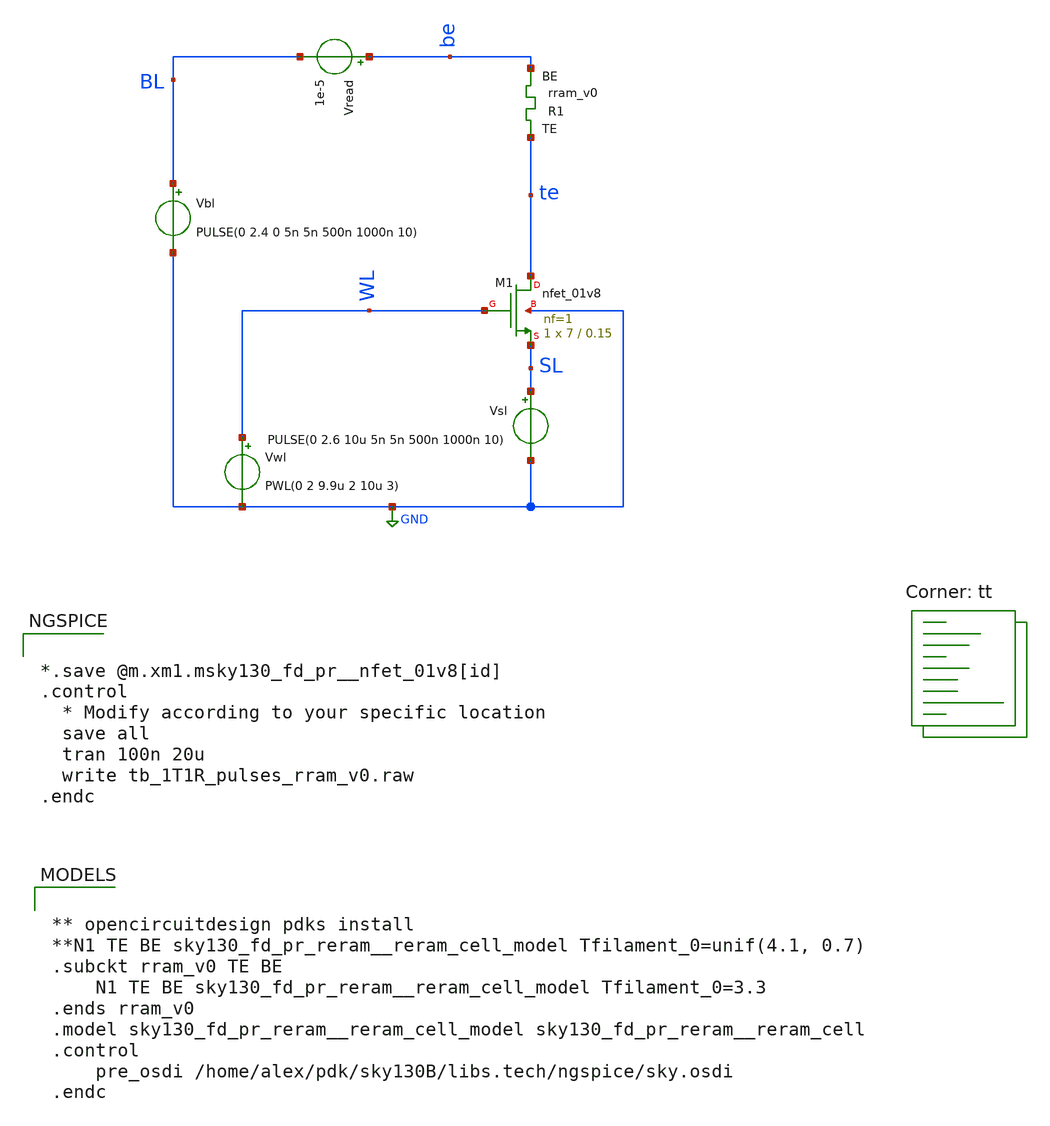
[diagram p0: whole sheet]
** sch_path: memristor_models/rram_london/tb_1T1R_pulses_sky.sch
**.subckt tb_1T1R_pulses_sky
XM1 te WL SL GND sky130_fd_pr__nfet_01v8 L=0.15 W=7 nf=1 ad='int((nf+1)/2) * W/nf * 0.29' as='int((nf+2)/2) * W/nf * 0.29'
+ pd='2*int((nf+1)/2) * (W/nf + 0.29)' ps='2*int((nf+2)/2) * (W/nf + 0.29)' nrd='0.29 / W' nrs='0.29 / W'
+ sa=0 sb=0 sd=0 mult=1 m=1
Vwl WL GND PWL(0 2 9.9u 2 10u 3)
Vbl BL GND PULSE(0 2.4 0 5n 5n 500n 1000n 10)
Vread be BL 1e-5
XR1 te be rram_v0
Vsl SL GND PULSE(0 2.6 10u 5n 5n 500n 1000n 10)
**** begin user architecture code


*.save @m.xm1.msky130_fd_pr__nfet_01v8[id]
.control
  * Modify according to your specific location
  save all
  tran 100n 20u
  write tb_1T1R_pulses_rram_v0.raw
.endc



.lib $::SKYWATER_MODELS/sky130.lib.spice tt

** opencircuitdesign pdks install
**N1 TE BE sky130_fd_pr_reram__reram_cell_model Tfilament_0=unif(4.1, 0.7)
.subckt rram_v0 TE BE
	N1 TE BE sky130_fd_pr_reram__reram_cell_model Tfilament_0=3.3
.ends rram_v0
.model sky130_fd_pr_reram__reram_cell_model sky130_fd_pr_reram__reram_cell
.control
	pre_osdi /home/alex/pdk/sky130B/libs.tech/ngspice/sky.osdi
.endc

**** end user architecture code
**.ends
.GLOBAL GND
.end
